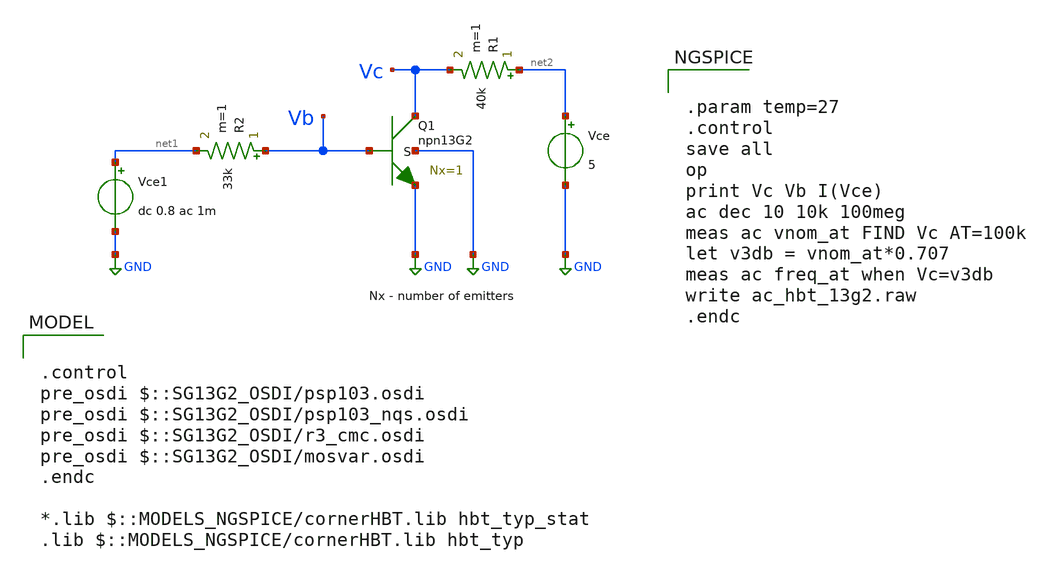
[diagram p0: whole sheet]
** sch_path: ihp-sg13g2/xschem_libs/sg13g2_tests/ac_hbt_13g2/schematic/ac_hbt_13g2.sch
* Copyright 2023 IHP PDK Authors
**.subckt ac_hbt_13g2
Vce net2 GND 5
XQ1 Vc Vb GND GND npn13G2 Nx=1 mm_ok=1
R1 net2 Vc 40k m=1
Vce1 net1 GND dc 0.8 ac 1m
R2 Vb net1 33k m=1
**** begin user architecture code

.control
pre_osdi $::SG13G2_OSDI/psp103.osdi
pre_osdi $::SG13G2_OSDI/psp103_nqs.osdi
pre_osdi $::SG13G2_OSDI/r3_cmc.osdi
pre_osdi $::SG13G2_OSDI/mosvar.osdi
.endc

*.lib $::MODELS_NGSPICE/cornerHBT.lib hbt_typ_stat
.lib $::MODELS_NGSPICE/cornerHBT.lib hbt_typ



.param temp=27
.control
save all
op
print Vc Vb I(Vce)
ac dec 10 10k 100meg
meas ac vnom_at FIND Vc AT=100k
let v3db = vnom_at*0.707
meas ac freq_at when Vc=v3db
write ac_hbt_13g2.raw
.endc


**** end user architecture code
**.ends
.GLOBAL GND
.end
